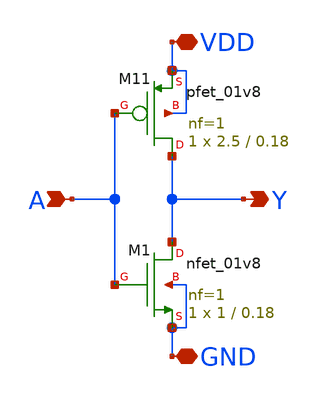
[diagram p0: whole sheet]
** sch_path: test_inv.sch
**.subckt test_inv A Y GND VDD
*.ipin A
*.opin Y
*.iopin GND
*.iopin VDD
XM1 Y A GND GND sky130_fd_pr__nfet_01v8 L=0.18 W=1 nf=1 ad='int((nf+1)/2) * W/nf * 0.29' as='int((nf+2)/2) * W/nf * 0.29'
+ pd='2*int((nf+1)/2) * (W/nf + 0.29)' ps='2*int((nf+2)/2) * (W/nf + 0.29)' nrd='0.29 / W' nrs='0.29 / W'
+ sa=0 sb=0 sd=0 mult=1 m=1
XM11 Y A VDD VDD sky130_fd_pr__pfet_01v8 L=0.18 W=2.5 nf=1 ad='int((nf+1)/2) * W/nf * 0.29' as='int((nf+2)/2) * W/nf * 0.29'
+ pd='2*int((nf+1)/2) * (W/nf + 0.29)' ps='2*int((nf+2)/2) * (W/nf + 0.29)' nrd='0.29 / W' nrs='0.29 / W'
+ sa=0 sb=0 sd=0 mult=1 m=1
**.ends
.end
